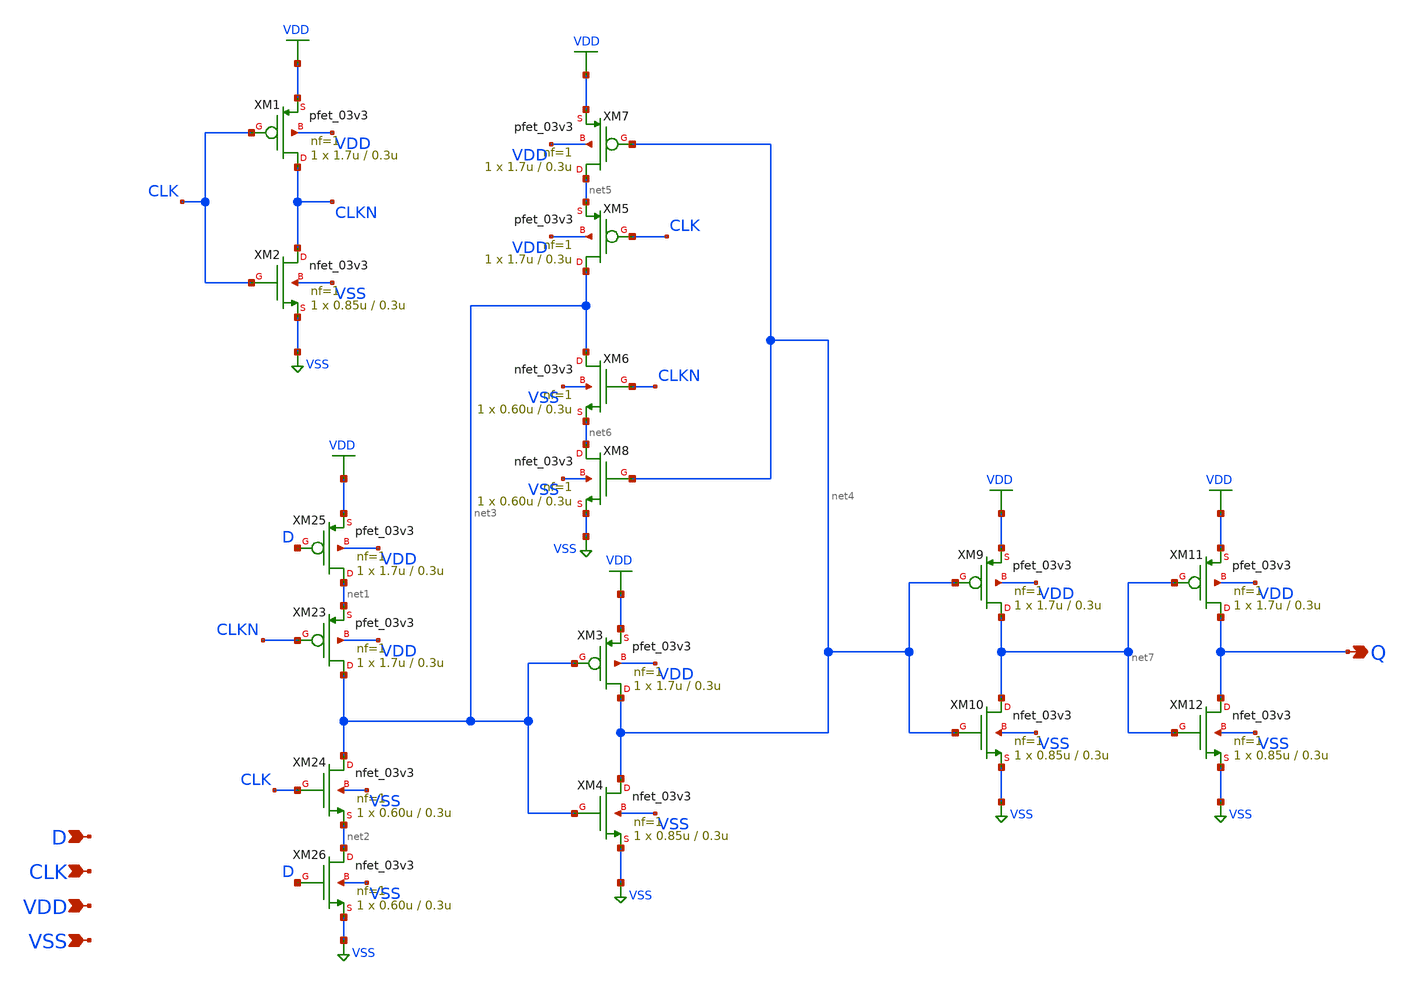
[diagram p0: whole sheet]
** sch_path: gf180mcu_osu_sc_gp9t3v3/xschem/gf180mcu_osu_sc_gp9t3v3__dlat_1.sch
**.subckt gf180mcu_osu_sc_gp9t3v3__dlat_1 D CLK Q VDD VSS
*.ipin D
*.ipin CLK
*.opin Q
*.ipin VDD
*.ipin VSS
XM1 CLKN CLK VDD VDD pfet_03v3 L=0.3u W=1.7u nf=1 ad='int((nf+1)/2) * W/nf * 0.18u' as='int((nf+2)/2) * W/nf * 0.18u'
+ pd='2*int((nf+1)/2) * (W/nf + 0.18u)' ps='2*int((nf+2)/2) * (W/nf + 0.18u)' nrd='0.18u / W' nrs='0.18u / W'
+ sa=0 sb=0 sd=0 m=1
XM2 CLKN CLK VSS VSS nfet_03v3 L=0.3u W=0.85u nf=1 ad='int((nf+1)/2) * W/nf * 0.18u' as='int((nf+2)/2) * W/nf * 0.18u'
+ pd='2*int((nf+1)/2) * (W/nf + 0.18u)' ps='2*int((nf+2)/2) * (W/nf + 0.18u)' nrd='0.18u / W' nrs='0.18u / W'
+ sa=0 sb=0 sd=0 m=1
XM23 net3 CLKN net1 VDD pfet_03v3 L=0.3u W=1.7u nf=1 ad='int((nf+1)/2) * W/nf * 0.18u' as='int((nf+2)/2) * W/nf * 0.18u'
+ pd='2*int((nf+1)/2) * (W/nf + 0.18u)' ps='2*int((nf+2)/2) * (W/nf + 0.18u)' nrd='0.18u / W' nrs='0.18u / W'
+ sa=0 sb=0 sd=0 m=1
XM24 net3 CLK net2 VSS nfet_03v3 L=0.3u W=0.60u nf=1 ad='int((nf+1)/2) * W/nf * 0.18u' as='int((nf+2)/2) * W/nf * 0.18u'
+ pd='2*int((nf+1)/2) * (W/nf + 0.18u)' ps='2*int((nf+2)/2) * (W/nf + 0.18u)' nrd='0.18u / W' nrs='0.18u / W'
+ sa=0 sb=0 sd=0 m=1
XM25 net1 D VDD VDD pfet_03v3 L=0.3u W=1.7u nf=1 ad='int((nf+1)/2) * W/nf * 0.18u' as='int((nf+2)/2) * W/nf * 0.18u'
+ pd='2*int((nf+1)/2) * (W/nf + 0.18u)' ps='2*int((nf+2)/2) * (W/nf + 0.18u)' nrd='0.18u / W' nrs='0.18u / W'
+ sa=0 sb=0 sd=0 m=1
XM26 net2 D VSS VSS nfet_03v3 L=0.3u W=0.60u nf=1 ad='int((nf+1)/2) * W/nf * 0.18u' as='int((nf+2)/2) * W/nf * 0.18u'
+ pd='2*int((nf+1)/2) * (W/nf + 0.18u)' ps='2*int((nf+2)/2) * (W/nf + 0.18u)' nrd='0.18u / W' nrs='0.18u / W'
+ sa=0 sb=0 sd=0 m=1
XM3 net4 net3 VDD VDD pfet_03v3 L=0.3u W=1.7u nf=1 ad='int((nf+1)/2) * W/nf * 0.18u' as='int((nf+2)/2) * W/nf * 0.18u'
+ pd='2*int((nf+1)/2) * (W/nf + 0.18u)' ps='2*int((nf+2)/2) * (W/nf + 0.18u)' nrd='0.18u / W' nrs='0.18u / W'
+ sa=0 sb=0 sd=0 m=1
XM4 net4 net3 VSS VSS nfet_03v3 L=0.3u W=0.85u nf=1 ad='int((nf+1)/2) * W/nf * 0.18u' as='int((nf+2)/2) * W/nf * 0.18u'
+ pd='2*int((nf+1)/2) * (W/nf + 0.18u)' ps='2*int((nf+2)/2) * (W/nf + 0.18u)' nrd='0.18u / W' nrs='0.18u / W'
+ sa=0 sb=0 sd=0 m=1
XM5 net3 CLK net5 VDD pfet_03v3 L=0.3u W=1.7u nf=1 ad='int((nf+1)/2) * W/nf * 0.18u' as='int((nf+2)/2) * W/nf * 0.18u'
+ pd='2*int((nf+1)/2) * (W/nf + 0.18u)' ps='2*int((nf+2)/2) * (W/nf + 0.18u)' nrd='0.18u / W' nrs='0.18u / W'
+ sa=0 sb=0 sd=0 m=1
XM6 net3 CLKN net6 VSS nfet_03v3 L=0.3u W=0.60u nf=1 ad='int((nf+1)/2) * W/nf * 0.18u' as='int((nf+2)/2) * W/nf * 0.18u'
+ pd='2*int((nf+1)/2) * (W/nf + 0.18u)' ps='2*int((nf+2)/2) * (W/nf + 0.18u)' nrd='0.18u / W' nrs='0.18u / W'
+ sa=0 sb=0 sd=0 m=1
XM7 net5 net4 VDD VDD pfet_03v3 L=0.3u W=1.7u nf=1 ad='int((nf+1)/2) * W/nf * 0.18u' as='int((nf+2)/2) * W/nf * 0.18u'
+ pd='2*int((nf+1)/2) * (W/nf + 0.18u)' ps='2*int((nf+2)/2) * (W/nf + 0.18u)' nrd='0.18u / W' nrs='0.18u / W'
+ sa=0 sb=0 sd=0 m=1
XM8 net6 net4 VSS VSS nfet_03v3 L=0.3u W=0.60u nf=1 ad='int((nf+1)/2) * W/nf * 0.18u' as='int((nf+2)/2) * W/nf * 0.18u'
+ pd='2*int((nf+1)/2) * (W/nf + 0.18u)' ps='2*int((nf+2)/2) * (W/nf + 0.18u)' nrd='0.18u / W' nrs='0.18u / W'
+ sa=0 sb=0 sd=0 m=1
XM9 net7 net4 VDD VDD pfet_03v3 L=0.3u W=1.7u nf=1 ad='int((nf+1)/2) * W/nf * 0.18u' as='int((nf+2)/2) * W/nf * 0.18u'
+ pd='2*int((nf+1)/2) * (W/nf + 0.18u)' ps='2*int((nf+2)/2) * (W/nf + 0.18u)' nrd='0.18u / W' nrs='0.18u / W'
+ sa=0 sb=0 sd=0 m=1
XM10 net7 net4 VSS VSS nfet_03v3 L=0.3u W=0.85u nf=1 ad='int((nf+1)/2) * W/nf * 0.18u' as='int((nf+2)/2) * W/nf * 0.18u'
+ pd='2*int((nf+1)/2) * (W/nf + 0.18u)' ps='2*int((nf+2)/2) * (W/nf + 0.18u)' nrd='0.18u / W' nrs='0.18u / W'
+ sa=0 sb=0 sd=0 m=1
XM11 Q net7 VDD VDD pfet_03v3 L=0.3u W=1.7u nf=1 ad='int((nf+1)/2) * W/nf * 0.18u' as='int((nf+2)/2) * W/nf * 0.18u'
+ pd='2*int((nf+1)/2) * (W/nf + 0.18u)' ps='2*int((nf+2)/2) * (W/nf + 0.18u)' nrd='0.18u / W' nrs='0.18u / W'
+ sa=0 sb=0 sd=0 m=1
XM12 Q net7 VSS VSS nfet_03v3 L=0.3u W=0.85u nf=1 ad='int((nf+1)/2) * W/nf * 0.18u' as='int((nf+2)/2) * W/nf * 0.18u'
+ pd='2*int((nf+1)/2) * (W/nf + 0.18u)' ps='2*int((nf+2)/2) * (W/nf + 0.18u)' nrd='0.18u / W' nrs='0.18u / W'
+ sa=0 sb=0 sd=0 m=1
**.ends
.GLOBAL VDD
.GLOBAL VSS
.end
